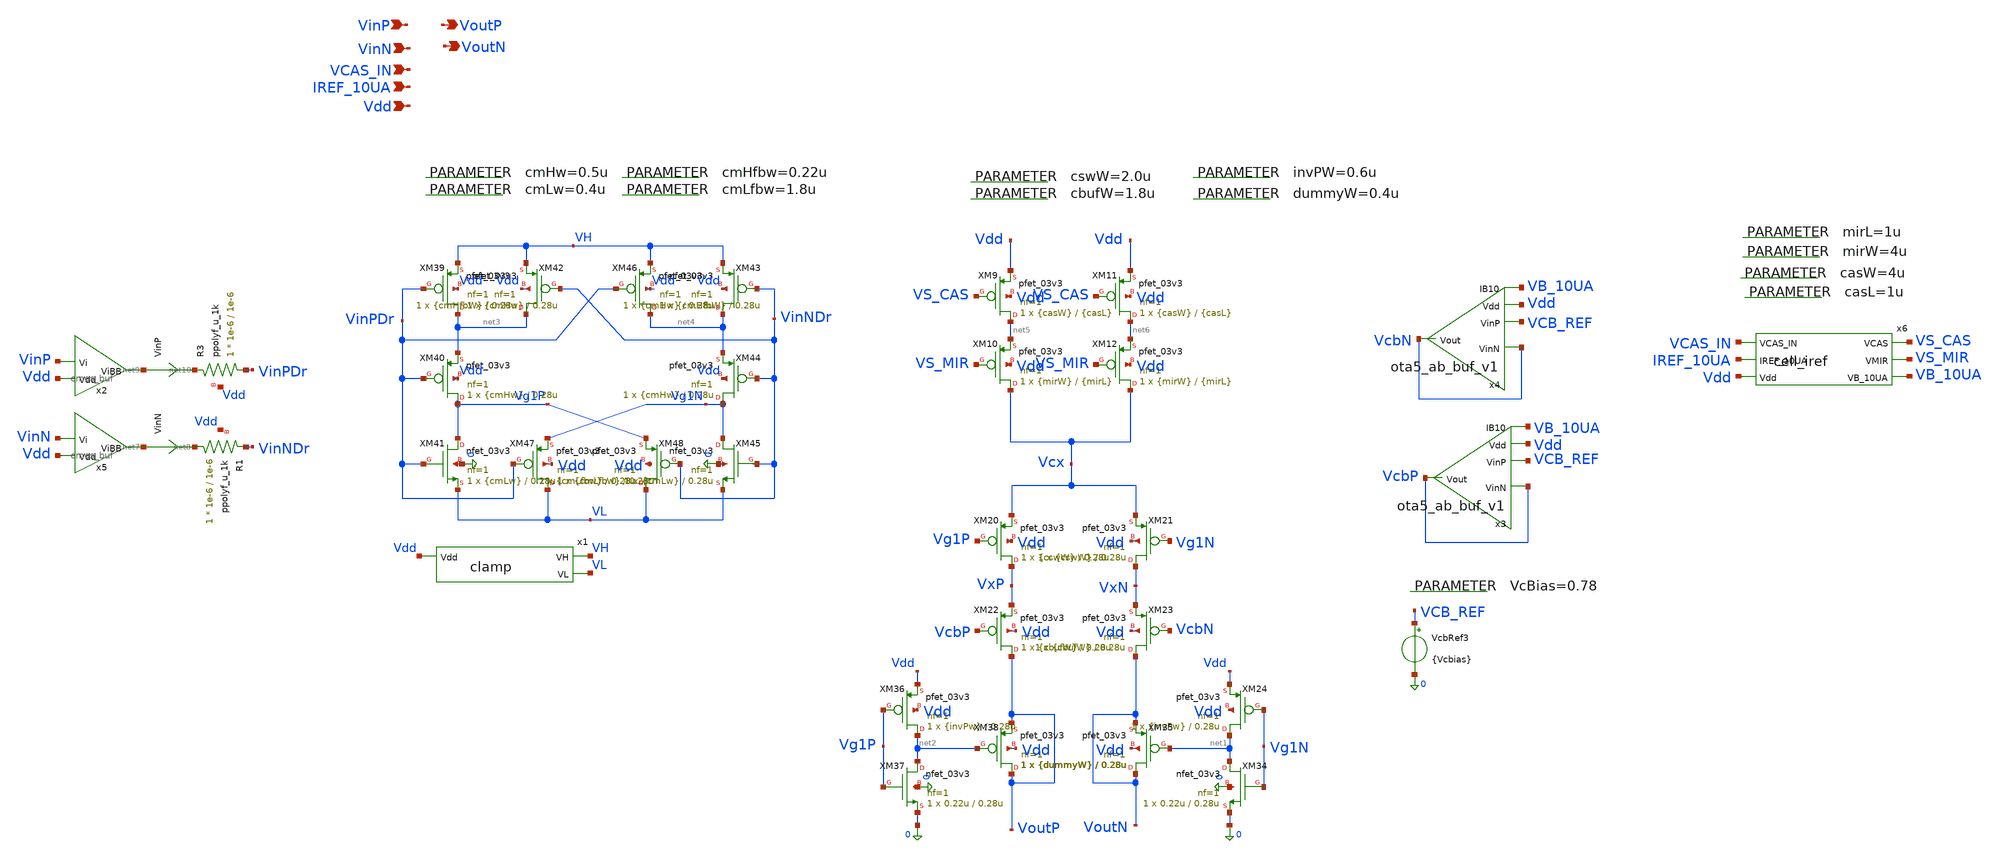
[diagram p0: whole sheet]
** sch_path: blocks/dac/cellv9/dac_cell_20ua_v9.sch
**.subckt dac_cell_20ua_v9 VoutP VoutN VinP VinN Vdd VCAS_IN IREF_10UA
*.opin VoutP
*.opin VoutN
*.ipin VinP
*.ipin VinN
*.ipin Vdd
*.ipin VCAS_IN
*.ipin IREF_10UA
.param cmLw=0.4u
.param cmHw=0.5u
.param cmLfbw=1.8u
.param cmHfbw=0.22u
XM20 VxP Vg1P Vcx Vdd pfet_03v3 L=0.28u W={cswW} nf=1 ad='int((nf+1)/2) * W/nf * 0.18u' as='int((nf+2)/2) * W/nf * 0.18u'
+ pd='2*int((nf+1)/2) * (W/nf + 0.18u)' ps='2*int((nf+2)/2) * (W/nf + 0.18u)' nrd='0.18u / W' nrs='0.18u / W'
+ sa=0 sb=0 sd=0 m=1
XM21 VxN Vg1N Vcx Vdd pfet_03v3 L=0.28u W={cswW} nf=1 ad='int((nf+1)/2) * W/nf * 0.18u' as='int((nf+2)/2) * W/nf * 0.18u'
+ pd='2*int((nf+1)/2) * (W/nf + 0.18u)' ps='2*int((nf+2)/2) * (W/nf + 0.18u)' nrd='0.18u / W' nrs='0.18u / W'
+ sa=0 sb=0 sd=0 m=1
XM22 VoutP VcbP VxP Vdd pfet_03v3 L=0.28u W={cbufW} nf=1 ad='int((nf+1)/2) * W/nf * 0.18u' as='int((nf+2)/2) * W/nf * 0.18u'
+ pd='2*int((nf+1)/2) * (W/nf + 0.18u)' ps='2*int((nf+2)/2) * (W/nf + 0.18u)' nrd='0.18u / W' nrs='0.18u / W'
+ sa=0 sb=0 sd=0 m=1
XM23 VoutN VcbN VxN Vdd pfet_03v3 L=0.28u W={cbufW} nf=1 ad='int((nf+1)/2) * W/nf * 0.18u' as='int((nf+2)/2) * W/nf * 0.18u'
+ pd='2*int((nf+1)/2) * (W/nf + 0.18u)' ps='2*int((nf+2)/2) * (W/nf + 0.18u)' nrd='0.18u / W' nrs='0.18u / W'
+ sa=0 sb=0 sd=0 m=1
XM24 net1 Vg1N Vdd Vdd pfet_03v3 L=0.28u W={invPw} nf=1 ad='int((nf+1)/2) * W/nf * 0.18u' as='int((nf+2)/2) * W/nf * 0.18u'
+ pd='2*int((nf+1)/2) * (W/nf + 0.18u)' ps='2*int((nf+2)/2) * (W/nf + 0.18u)' nrd='0.18u / W' nrs='0.18u / W'
+ sa=0 sb=0 sd=0 m=1
XM34 net1 Vg1N 0 0 nfet_03v3 L=0.28u W=0.22u nf=1 ad='int((nf+1)/2) * W/nf * 0.18u' as='int((nf+2)/2) * W/nf * 0.18u'
+ pd='2*int((nf+1)/2) * (W/nf + 0.18u)' ps='2*int((nf+2)/2) * (W/nf + 0.18u)' nrd='0.18u / W' nrs='0.18u / W'
+ sa=0 sb=0 sd=0 m=1
XM35 VoutN net1 VoutN Vdd pfet_03v3 L=0.28u W={dummyW} nf=1 ad='int((nf+1)/2) * W/nf * 0.18u' as='int((nf+2)/2) * W/nf * 0.18u'
+ pd='2*int((nf+1)/2) * (W/nf + 0.18u)' ps='2*int((nf+2)/2) * (W/nf + 0.18u)' nrd='0.18u / W' nrs='0.18u / W'
+ sa=0 sb=0 sd=0 m=1
XM36 net2 Vg1P Vdd Vdd pfet_03v3 L=0.28u W={invPw} nf=1 ad='int((nf+1)/2) * W/nf * 0.18u' as='int((nf+2)/2) * W/nf * 0.18u'
+ pd='2*int((nf+1)/2) * (W/nf + 0.18u)' ps='2*int((nf+2)/2) * (W/nf + 0.18u)' nrd='0.18u / W' nrs='0.18u / W'
+ sa=0 sb=0 sd=0 m=1
XM37 net2 Vg1P 0 0 nfet_03v3 L=0.28u W=0.22u nf=1 ad='int((nf+1)/2) * W/nf * 0.18u' as='int((nf+2)/2) * W/nf * 0.18u'
+ pd='2*int((nf+1)/2) * (W/nf + 0.18u)' ps='2*int((nf+2)/2) * (W/nf + 0.18u)' nrd='0.18u / W' nrs='0.18u / W'
+ sa=0 sb=0 sd=0 m=1
XM38 VoutP net2 VoutP Vdd pfet_03v3 L=0.28u W={dummyW} nf=1 ad='int((nf+1)/2) * W/nf * 0.18u' as='int((nf+2)/2) * W/nf * 0.18u'
+ pd='2*int((nf+1)/2) * (W/nf + 0.18u)' ps='2*int((nf+2)/2) * (W/nf + 0.18u)' nrd='0.18u / W' nrs='0.18u / W'
+ sa=0 sb=0 sd=0 m=1
VcbRef3 VCB_REF 0 {Vcbias}
.save i(vcbref3)
.param VcBias=0.78
x3 Vdd VcbP VCB_REF VcbP VB_10UA ota5_ab_buf_v1
x4 Vdd VcbN VCB_REF VcbN VB_10UA ota5_ab_buf_v1
XM39 net3 VinPDr VH Vdd pfet_03v3 L=0.28u W={cmHw} nf=1 ad='int((nf+1)/2) * W/nf * 0.18u' as='int((nf+2)/2) * W/nf * 0.18u'
+ pd='2*int((nf+1)/2) * (W/nf + 0.18u)' ps='2*int((nf+2)/2) * (W/nf + 0.18u)' nrd='0.18u / W' nrs='0.18u / W'
+ sa=0 sb=0 sd=0 m=1
XM40 Vg1P VinPDr net3 Vdd pfet_03v3 L=0.28u W={cmHw} nf=1 ad='int((nf+1)/2) * W/nf * 0.18u' as='int((nf+2)/2) * W/nf * 0.18u'
+ pd='2*int((nf+1)/2) * (W/nf + 0.18u)' ps='2*int((nf+2)/2) * (W/nf + 0.18u)' nrd='0.18u / W' nrs='0.18u / W'
+ sa=0 sb=0 sd=0 m=1
XM41 Vg1P VinPDr VL 0 nfet_03v3 L=0.28u W={cmLw} nf=1 ad='int((nf+1)/2) * W/nf * 0.18u' as='int((nf+2)/2) * W/nf * 0.18u'
+ pd='2*int((nf+1)/2) * (W/nf + 0.18u)' ps='2*int((nf+2)/2) * (W/nf + 0.18u)' nrd='0.18u / W' nrs='0.18u / W'
+ sa=0 sb=0 sd=0 m=1
XM42 net3 VinNDr VH Vdd pfet_03v3 L=0.28u W={cmHfbW} nf=1 ad='int((nf+1)/2) * W/nf * 0.18u' as='int((nf+2)/2) * W/nf * 0.18u'
+ pd='2*int((nf+1)/2) * (W/nf + 0.18u)' ps='2*int((nf+2)/2) * (W/nf + 0.18u)' nrd='0.18u / W' nrs='0.18u / W'
+ sa=0 sb=0 sd=0 m=1
XM43 net4 VinNDr VH Vdd pfet_03v3 L=0.28u W={cmHw} nf=1 ad='int((nf+1)/2) * W/nf * 0.18u' as='int((nf+2)/2) * W/nf * 0.18u'
+ pd='2*int((nf+1)/2) * (W/nf + 0.18u)' ps='2*int((nf+2)/2) * (W/nf + 0.18u)' nrd='0.18u / W' nrs='0.18u / W'
+ sa=0 sb=0 sd=0 m=1
XM44 Vg1N VinNDr net4 Vdd pfet_03v3 L=0.28u W={cmHw} nf=1 ad='int((nf+1)/2) * W/nf * 0.18u' as='int((nf+2)/2) * W/nf * 0.18u'
+ pd='2*int((nf+1)/2) * (W/nf + 0.18u)' ps='2*int((nf+2)/2) * (W/nf + 0.18u)' nrd='0.18u / W' nrs='0.18u / W'
+ sa=0 sb=0 sd=0 m=1
XM45 Vg1N VinNDr VL 0 nfet_03v3 L=0.28u W={cmLw} nf=1 ad='int((nf+1)/2) * W/nf * 0.18u' as='int((nf+2)/2) * W/nf * 0.18u'
+ pd='2*int((nf+1)/2) * (W/nf + 0.18u)' ps='2*int((nf+2)/2) * (W/nf + 0.18u)' nrd='0.18u / W' nrs='0.18u / W'
+ sa=0 sb=0 sd=0 m=1
XM46 net4 VinPDr VH Vdd pfet_03v3 L=0.28u W={cmHfbW} nf=1 ad='int((nf+1)/2) * W/nf * 0.18u' as='int((nf+2)/2) * W/nf * 0.18u'
+ pd='2*int((nf+1)/2) * (W/nf + 0.18u)' ps='2*int((nf+2)/2) * (W/nf + 0.18u)' nrd='0.18u / W' nrs='0.18u / W'
+ sa=0 sb=0 sd=0 m=1
XM47 VL VinPDr Vg1N Vdd pfet_03v3 L=0.28u W={cmLfbw} nf=1 ad='int((nf+1)/2) * W/nf * 0.18u' as='int((nf+2)/2) * W/nf * 0.18u'
+ pd='2*int((nf+1)/2) * (W/nf + 0.18u)' ps='2*int((nf+2)/2) * (W/nf + 0.18u)' nrd='0.18u / W' nrs='0.18u / W'
+ sa=0 sb=0 sd=0 m=1
XM48 VL VinNDr Vg1P Vdd pfet_03v3 L=0.28u W={cmLfbw} nf=1 ad='int((nf+1)/2) * W/nf * 0.18u' as='int((nf+2)/2) * W/nf * 0.18u'
+ pd='2*int((nf+1)/2) * (W/nf + 0.18u)' ps='2*int((nf+2)/2) * (W/nf + 0.18u)' nrd='0.18u / W' nrs='0.18u / W'
+ sa=0 sb=0 sd=0 m=1
.param dummyW=0.4u
.param invPW=0.6u
.param cswW=2.0u
.param cbufW=1.8u
x1 VH Vdd VL clamp
XM9 net5 VS_CAS Vdd Vdd pfet_03v3 L={casL} W={casW} nf=1 ad='int((nf+1)/2) * W/nf * 0.18u' as='int((nf+2)/2) * W/nf * 0.18u'
+ pd='2*int((nf+1)/2) * (W/nf + 0.18u)' ps='2*int((nf+2)/2) * (W/nf + 0.18u)' nrd='0.18u / W' nrs='0.18u / W'
+ sa=0 sb=0 sd=0 m=1
XM10 Vcx VS_MIR net5 Vdd pfet_03v3 L={mirL} W={mirW} nf=1 ad='int((nf+1)/2) * W/nf * 0.18u' as='int((nf+2)/2) * W/nf * 0.18u'
+ pd='2*int((nf+1)/2) * (W/nf + 0.18u)' ps='2*int((nf+2)/2) * (W/nf + 0.18u)' nrd='0.18u / W' nrs='0.18u / W'
+ sa=0 sb=0 sd=0 m=1
XM11 net6 VS_CAS Vdd Vdd pfet_03v3 L={casL} W={casW} nf=1 ad='int((nf+1)/2) * W/nf * 0.18u' as='int((nf+2)/2) * W/nf * 0.18u'
+ pd='2*int((nf+1)/2) * (W/nf + 0.18u)' ps='2*int((nf+2)/2) * (W/nf + 0.18u)' nrd='0.18u / W' nrs='0.18u / W'
+ sa=0 sb=0 sd=0 m=1
XM12 Vcx VS_MIR net6 Vdd pfet_03v3 L={mirL} W={mirW} nf=1 ad='int((nf+1)/2) * W/nf * 0.18u' as='int((nf+2)/2) * W/nf * 0.18u'
+ pd='2*int((nf+1)/2) * (W/nf + 0.18u)' ps='2*int((nf+2)/2) * (W/nf + 0.18u)' nrd='0.18u / W' nrs='0.18u / W'
+ sa=0 sb=0 sd=0 m=1
VinN net7 net8 0
.save i(vinn)
x5 net7 VinN Vdd cmos_buf
VinP net9 net10 0
.save i(vinp)
x2 net9 VinP Vdd cmos_buf
XR3 VinPDr net10 Vdd ppolyf_u_1k r_width=1e-6 r_length=1e-6 m=1
XR1 net8 VinNDr Vdd ppolyf_u_1k r_width=1e-6 r_length=1e-6 m=1
.param casW=4u
.param mirW=4u
.param mirL=1u
.param casL=1u
x6 VCAS_IN VS_CAS VS_MIR IREF_10UA Vdd VB_10UA cell_iref
**.ends

* expanding   symbol:  cellv9/ota5_ab_buf_v1.sym # of pins=5
** sym_path: blocks/dac/cellv9/ota5_ab_buf_v1.sym
** sch_path: blocks/dac/cellv9/ota5_ab_buf_v1.sch
.subckt ota5_ab_buf_v1 Vdd VinN VinP Vout IB10
*.opin Vout
*.ipin VinP
*.ipin VinN
*.ipin Vdd
*.ipin IB10
XM16 VoOTA net2 0 0 nfet_03v3 L=1u W=10u nf=1 ad='int((nf+1)/2) * W/nf * 0.18u' as='int((nf+2)/2) * W/nf * 0.18u'
+ pd='2*int((nf+1)/2) * (W/nf + 0.18u)' ps='2*int((nf+2)/2) * (W/nf + 0.18u)' nrd='0.18u / W' nrs='0.18u / W'
+ sa=0 sb=0 sd=0 m=1
XM18 VoOTA VinN net1 Vdd pfet_03v3 L=1u W=20u nf=1 ad='int((nf+1)/2) * W/nf * 0.18u' as='int((nf+2)/2) * W/nf * 0.18u'
+ pd='2*int((nf+1)/2) * (W/nf + 0.18u)' ps='2*int((nf+2)/2) * (W/nf + 0.18u)' nrd='0.18u / W' nrs='0.18u / W'
+ sa=0 sb=0 sd=0 m=1
XM19 net2 VinP net1 Vdd pfet_03v3 L=1u W=20u nf=1 ad='int((nf+1)/2) * W/nf * 0.18u' as='int((nf+2)/2) * W/nf * 0.18u'
+ pd='2*int((nf+1)/2) * (W/nf + 0.18u)' ps='2*int((nf+2)/2) * (W/nf + 0.18u)' nrd='0.18u / W' nrs='0.18u / W'
+ sa=0 sb=0 sd=0 m=1
XM22 net2 net2 0 0 nfet_03v3 L=1u W=10u nf=1 ad='int((nf+1)/2) * W/nf * 0.18u' as='int((nf+2)/2) * W/nf * 0.18u'
+ pd='2*int((nf+1)/2) * (W/nf + 0.18u)' ps='2*int((nf+2)/2) * (W/nf + 0.18u)' nrd='0.18u / W' nrs='0.18u / W'
+ sa=0 sb=0 sd=0 m=1
XM1 net1 net3 Vdd Vdd pfet_03v3 L=1u W=40u nf=1 ad='int((nf+1)/2) * W/nf * 0.18u' as='int((nf+2)/2) * W/nf * 0.18u'
+ pd='2*int((nf+1)/2) * (W/nf + 0.18u)' ps='2*int((nf+2)/2) * (W/nf + 0.18u)' nrd='0.18u / W' nrs='0.18u / W'
+ sa=0 sb=0 sd=0 m=1
XM2 net3 net3 Vdd Vdd pfet_03v3 L=1u W=40u nf=1 ad='int((nf+1)/2) * W/nf * 0.18u' as='int((nf+2)/2) * W/nf * 0.18u'
+ pd='2*int((nf+1)/2) * (W/nf + 0.18u)' ps='2*int((nf+2)/2) * (W/nf + 0.18u)' nrd='0.18u / W' nrs='0.18u / W'
+ sa=0 sb=0 sd=0 m=1
XM3 VI1b VI1a VI2 Vdd pfet_03v3 L=0.5u W=40u nf=1 ad='int((nf+1)/2) * W/nf * 0.18u' as='int((nf+2)/2) * W/nf * 0.18u'
+ pd='2*int((nf+1)/2) * (W/nf + 0.18u)' ps='2*int((nf+2)/2) * (W/nf + 0.18u)' nrd='0.18u / W' nrs='0.18u / W'
+ sa=0 sb=0 sd=0 m=1
XM4 VI2 VoOTA Vout 0 nfet_03v3 L=0.5u W=80u nf=1 ad='int((nf+1)/2) * W/nf * 0.18u' as='int((nf+2)/2) * W/nf * 0.18u'
+ pd='2*int((nf+1)/2) * (W/nf + 0.18u)' ps='2*int((nf+2)/2) * (W/nf + 0.18u)' nrd='0.18u / W' nrs='0.18u / W'
+ sa=0 sb=0 sd=0 m=1
XM5 Vout VI2 Vdd Vdd pfet_03v3 L=1u W=80u nf=1 ad='int((nf+1)/2) * W/nf * 0.18u' as='int((nf+2)/2) * W/nf * 0.18u'
+ pd='2*int((nf+1)/2) * (W/nf + 0.18u)' ps='2*int((nf+2)/2) * (W/nf + 0.18u)' nrd='0.18u / W' nrs='0.18u / W'
+ sa=0 sb=0 sd=0 m=1
XM6 Vout VI1b 0 0 nfet_03v3 L=0.5u W=40u nf=1 ad='int((nf+1)/2) * W/nf * 0.18u' as='int((nf+2)/2) * W/nf * 0.18u'
+ pd='2*int((nf+1)/2) * (W/nf + 0.18u)' ps='2*int((nf+2)/2) * (W/nf + 0.18u)' nrd='0.18u / W' nrs='0.18u / W'
+ sa=0 sb=0 sd=0 m=1
XM7 VI1a VI1a VI0 Vdd pfet_03v3 L=0.5u W=40u nf=1 ad='int((nf+1)/2) * W/nf * 0.18u' as='int((nf+2)/2) * W/nf * 0.18u'
+ pd='2*int((nf+1)/2) * (W/nf + 0.18u)' ps='2*int((nf+2)/2) * (W/nf + 0.18u)' nrd='0.18u / W' nrs='0.18u / W'
+ sa=0 sb=0 sd=0 m=1
XM8 VI1a VI0 Vdd Vdd pfet_03v3 L=1u W=80u nf=1 ad='int((nf+1)/2) * W/nf * 0.18u' as='int((nf+2)/2) * W/nf * 0.18u'
+ pd='2*int((nf+1)/2) * (W/nf + 0.18u)' ps='2*int((nf+2)/2) * (W/nf + 0.18u)' nrd='0.18u / W' nrs='0.18u / W'
+ sa=0 sb=0 sd=0 m=1
XM11 VI0 net4 Vdd Vdd pfet_03v3 L=0.5u W=80u nf=1 ad='int((nf+1)/2) * W/nf * 0.18u' as='int((nf+2)/2) * W/nf * 0.18u'
+ pd='2*int((nf+1)/2) * (W/nf + 0.18u)' ps='2*int((nf+2)/2) * (W/nf + 0.18u)' nrd='0.18u / W' nrs='0.18u / W'
+ sa=0 sb=0 sd=0 m=1
XM12 net4 net4 Vdd Vdd pfet_03v3 L=0.5u W=80u nf=1 ad='int((nf+1)/2) * W/nf * 0.18u' as='int((nf+2)/2) * W/nf * 0.18u'
+ pd='2*int((nf+1)/2) * (W/nf + 0.18u)' ps='2*int((nf+2)/2) * (W/nf + 0.18u)' nrd='0.18u / W' nrs='0.18u / W'
+ sa=0 sb=0 sd=0 m=1
XM9 VI2 net4 Vdd Vdd pfet_03v3 L=0.5u W=80u nf=1 ad='int((nf+1)/2) * W/nf * 0.18u' as='int((nf+2)/2) * W/nf * 0.18u'
+ pd='2*int((nf+1)/2) * (W/nf + 0.18u)' ps='2*int((nf+2)/2) * (W/nf + 0.18u)' nrd='0.18u / W' nrs='0.18u / W'
+ sa=0 sb=0 sd=0 m=1
XM10 net5 net5 Vdd Vdd pfet_03v3 L=0.5u W=40u nf=1 ad='int((nf+1)/2) * W/nf * 0.18u' as='int((nf+2)/2) * W/nf * 0.18u'
+ pd='2*int((nf+1)/2) * (W/nf + 0.18u)' ps='2*int((nf+2)/2) * (W/nf + 0.18u)' nrd='0.18u / W' nrs='0.18u / W'
+ sa=0 sb=0 sd=0 m=1
XM15 IB30Ref net5 Vdd Vdd pfet_03v3 L=0.5u W=40u nf=1 ad='int((nf+1)/2) * W/nf * 0.18u' as='int((nf+2)/2) * W/nf * 0.18u'
+ pd='2*int((nf+1)/2) * (W/nf + 0.18u)' ps='2*int((nf+2)/2) * (W/nf + 0.18u)' nrd='0.18u / W' nrs='0.18u / W'
+ sa=0 sb=0 sd=0 m=1
XM17 IB30Ref IB30Ref 0 0 nfet_03v3 L=0.5u W=40u nf=1 ad='int((nf+1)/2) * W/nf * 0.18u' as='int((nf+2)/2) * W/nf * 0.18u'
+ pd='2*int((nf+1)/2) * (W/nf + 0.18u)' ps='2*int((nf+2)/2) * (W/nf + 0.18u)' nrd='0.18u / W' nrs='0.18u / W'
+ sa=0 sb=0 sd=0 m=1
XM20 VI1a IB30Ref 0 0 nfet_03v3 L=0.5u W=40u nf=1 ad='int((nf+1)/2) * W/nf * 0.18u' as='int((nf+2)/2) * W/nf * 0.18u'
+ pd='2*int((nf+1)/2) * (W/nf + 0.18u)' ps='2*int((nf+2)/2) * (W/nf + 0.18u)' nrd='0.18u / W' nrs='0.18u / W'
+ sa=0 sb=0 sd=0 m=1
XM21 VI1b IB30Ref 0 0 nfet_03v3 L=0.5u W=40u nf=1 ad='int((nf+1)/2) * W/nf * 0.18u' as='int((nf+2)/2) * W/nf * 0.18u'
+ pd='2*int((nf+1)/2) * (W/nf + 0.18u)' ps='2*int((nf+2)/2) * (W/nf + 0.18u)' nrd='0.18u / W' nrs='0.18u / W'
+ sa=0 sb=0 sd=0 m=2
XM13 net4 IB30Ref 0 0 nfet_03v3 L=0.5u W=40u nf=1 ad='int((nf+1)/2) * W/nf * 0.18u' as='int((nf+2)/2) * W/nf * 0.18u'
+ pd='2*int((nf+1)/2) * (W/nf + 0.18u)' ps='2*int((nf+2)/2) * (W/nf + 0.18u)' nrd='0.18u / W' nrs='0.18u / W'
+ sa=0 sb=0 sd=0 m=2
XM30 net3 IB10 0 0 nfet_03v3 L=1u W=8u nf=1 ad='int((nf+1)/2) * W/nf * 0.18u' as='int((nf+2)/2) * W/nf * 0.18u'
+ pd='2*int((nf+1)/2) * (W/nf + 0.18u)' ps='2*int((nf+2)/2) * (W/nf + 0.18u)' nrd='0.18u / W' nrs='0.18u / W'
+ sa=0 sb=0 sd=0 m=2
XM14 net5 IB10 0 0 nfet_03v3 L=1u W=8u nf=1 ad='int((nf+1)/2) * W/nf * 0.18u' as='int((nf+2)/2) * W/nf * 0.18u'
+ pd='2*int((nf+1)/2) * (W/nf + 0.18u)' ps='2*int((nf+2)/2) * (W/nf + 0.18u)' nrd='0.18u / W' nrs='0.18u / W'
+ sa=0 sb=0 sd=0 m=3
.ends


* expanding   symbol:  cellv9/clamp.sym # of pins=3
** sym_path: blocks/dac/cellv9/clamp.sym
** sch_path: blocks/dac/cellv9/clamp.sch
.subckt clamp VH Vdd VL
*.opin VH
*.opin VL
*.ipin Vdd
XM49 VL FB 0 0 nfet_03v3 L=0.28u W=2u nf=1 ad='int((nf+1)/2) * W/nf * 0.18u' as='int((nf+2)/2) * W/nf * 0.18u'
+ pd='2*int((nf+1)/2) * (W/nf + 0.18u)' ps='2*int((nf+2)/2) * (W/nf + 0.18u)' nrd='0.18u / W' nrs='0.18u / W'
+ sa=0 sb=0 sd=0 m=1
XM50 VH FB Vdd Vdd pfet_03v3 L=0.28u W=4u nf=1 ad='int((nf+1)/2) * W/nf * 0.18u' as='int((nf+2)/2) * W/nf * 0.18u'
+ pd='2*int((nf+1)/2) * (W/nf + 0.18u)' ps='2*int((nf+2)/2) * (W/nf + 0.18u)' nrd='0.18u / W' nrs='0.18u / W'
+ sa=0 sb=0 sd=0 m=1
XR3 VL FB Vdd ppolyf_u_1k r_width=1e-6 r_length=1e-6 m=1
XR1 FB VH Vdd ppolyf_u_1k r_width=1e-6 r_length=15e-6 m=1
XC2 Vdd VH cap_mim_2f0_m3m4_noshield c_width=25e-6 c_length=20e-6 m=1
XC1 Vdd VH cap_mim_2f0_m3m4_noshield c_width=10e-6 c_length=5e-6 m=1
XC3 Vdd VH cap_mim_2f0_m3m4_noshield c_width=5e-6 c_length=5e-6 m=1
XC4 VL 0 cap_mim_2f0_m3m4_noshield c_width=25e-6 c_length=20e-6 m=1
XC5 VL 0 cap_mim_2f0_m3m4_noshield c_width=10e-6 c_length=5e-6 m=1
XC6 VL 0 cap_mim_2f0_m3m4_noshield c_width=5e-6 c_length=5e-6 m=1
XC7 Vdd 0 cap_mim_2f0_m3m4_noshield c_width=25e-6 c_length=20e-6 m=1
XC8 FB 0 cap_mim_2f0_m3m4_noshield c_width=10e-6 c_length=5e-6 m=8
.ends


* expanding   symbol:  common/cmos_buf.sym # of pins=3
** sym_path: blocks/dac/common/cmos_buf.sym
** sch_path: blocks/dac/common/cmos_buf.sch
.subckt cmos_buf ViBB Vi Vdd
*.ipin Vi
*.opin ViBB
*.ipin Vdd
XM49 ViB Vi 0 0 nfet_03v3 L=0.28u W=0.5u nf=1 ad='int((nf+1)/2) * W/nf * 0.18u' as='int((nf+2)/2) * W/nf * 0.18u'
+ pd='2*int((nf+1)/2) * (W/nf + 0.18u)' ps='2*int((nf+2)/2) * (W/nf + 0.18u)' nrd='0.18u / W' nrs='0.18u / W'
+ sa=0 sb=0 sd=0 m=1
XM50 ViB Vi Vdd Vdd pfet_03v3 L=0.28u W=1u nf=1 ad='int((nf+1)/2) * W/nf * 0.18u' as='int((nf+2)/2) * W/nf * 0.18u'
+ pd='2*int((nf+1)/2) * (W/nf + 0.18u)' ps='2*int((nf+2)/2) * (W/nf + 0.18u)' nrd='0.18u / W' nrs='0.18u / W'
+ sa=0 sb=0 sd=0 m=1
XM1 ViBB ViB 0 0 nfet_03v3 L=0.28u W=0.5u nf=1 ad='int((nf+1)/2) * W/nf * 0.18u' as='int((nf+2)/2) * W/nf * 0.18u'
+ pd='2*int((nf+1)/2) * (W/nf + 0.18u)' ps='2*int((nf+2)/2) * (W/nf + 0.18u)' nrd='0.18u / W' nrs='0.18u / W'
+ sa=0 sb=0 sd=0 m=1
XM2 ViBB ViB Vdd Vdd pfet_03v3 L=0.28u W=1u nf=1 ad='int((nf+1)/2) * W/nf * 0.18u' as='int((nf+2)/2) * W/nf * 0.18u'
+ pd='2*int((nf+1)/2) * (W/nf + 0.18u)' ps='2*int((nf+2)/2) * (W/nf + 0.18u)' nrd='0.18u / W' nrs='0.18u / W'
+ sa=0 sb=0 sd=0 m=1
.ends


* expanding   symbol:  cellv9/cell_iref.sym # of pins=6
** sym_path: blocks/dac/cellv9/cell_iref.sym
** sch_path: blocks/dac/cellv9/cell_iref.sch
.subckt cell_iref VCAS_IN VCAS VMIR IREF_10UA Vdd VB_10UA
*.opin VMIR
*.opin VCAS
*.ipin Vdd
*.ipin VCAS_IN
*.ipin IREF_10UA
*.opin VB_10UA
XM1 IREF_10UA IREF_10UA net1 Vdd pfet_03v3 L={mirL} W={mirW} nf=1 ad='int((nf+1)/2) * W/nf * 0.18u' as='int((nf+2)/2) * W/nf * 0.18u'
+ pd='2*int((nf+1)/2) * (W/nf + 0.18u)' ps='2*int((nf+2)/2) * (W/nf + 0.18u)' nrd='0.18u / W' nrs='0.18u / W'
+ sa=0 sb=0 sd=0 m=1
XM49 net1 VCAS Vdd Vdd pfet_03v3 L={casL} W={casW} nf=1 ad='int((nf+1)/2) * W/nf * 0.18u' as='int((nf+2)/2) * W/nf * 0.18u'
+ pd='2*int((nf+1)/2) * (W/nf + 0.18u)' ps='2*int((nf+2)/2) * (W/nf + 0.18u)' nrd='0.18u / W' nrs='0.18u / W'
+ sa=0 sb=0 sd=0 m=1
XM8 VB_10UA VMIR net2 Vdd pfet_03v3 L={mirL} W={mirW} nf=1 ad='int((nf+1)/2) * W/nf * 0.18u' as='int((nf+2)/2) * W/nf * 0.18u'
+ pd='2*int((nf+1)/2) * (W/nf + 0.18u)' ps='2*int((nf+2)/2) * (W/nf + 0.18u)' nrd='0.18u / W' nrs='0.18u / W'
+ sa=0 sb=0 sd=0 m=1
XM25 net2 VCAS Vdd Vdd pfet_03v3 L={casL} W={casW} nf=1 ad='int((nf+1)/2) * W/nf * 0.18u' as='int((nf+2)/2) * W/nf * 0.18u'
+ pd='2*int((nf+1)/2) * (W/nf + 0.18u)' ps='2*int((nf+2)/2) * (W/nf + 0.18u)' nrd='0.18u / W' nrs='0.18u / W'
+ sa=0 sb=0 sd=0 m=1
XM26 VB_10UA VB_10UA 0 0 nfet_03v3 L=1u W=8u nf=1 ad='int((nf+1)/2) * W/nf * 0.18u' as='int((nf+2)/2) * W/nf * 0.18u'
+ pd='2*int((nf+1)/2) * (W/nf + 0.18u)' ps='2*int((nf+2)/2) * (W/nf + 0.18u)' nrd='0.18u / W' nrs='0.18u / W'
+ sa=0 sb=0 sd=0 m=1
XR4 VCAS_IN VCAS Vdd ppolyf_u_1k r_width=2e-6 r_length=10e-6 m=1
XC1 VCAS 0 cap_mim_2f0_m3m4_noshield c_width=5e-6 c_length=5e-6 m=1
.param casW=4u
.param mirW=4u
.param mirL=1u
.param casL=1u
XR1 IREF_10UA VMIR Vdd ppolyf_u_1k r_width=2e-6 r_length=10e-6 m=1
XC2 VMIR 0 cap_mim_2f0_m3m4_noshield c_width=5e-6 c_length=5e-6 m=1
.ends

.end
